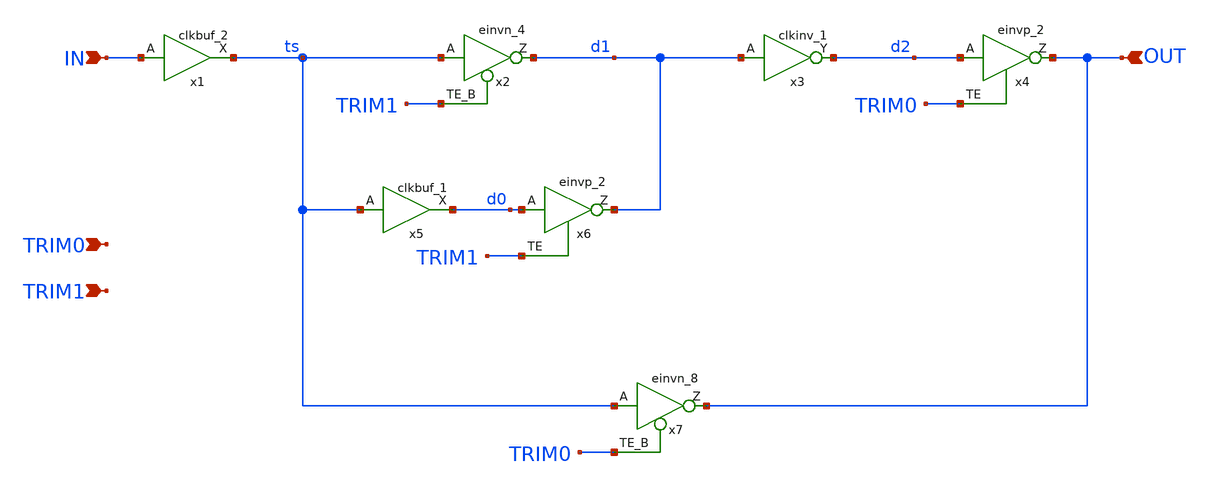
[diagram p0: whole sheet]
** sch_path: ip/randsack/sch/triminv.sch
**.subckt triminv IN OUT TRIM0 TRIM1
*.ipin IN
*.ipin OUT
*.ipin TRIM0
*.ipin TRIM1
x1 IN VGND VNB VPB VPWR ts sky130_fd_sc_hd__clkbuf_2
x2 ts TRIM1 VGND VNB VPB VPWR d1 sky130_fd_sc_hd__einvn_4
x3 d1 VGND VNB VPB VPWR d2 sky130_fd_sc_hd__clkinv_1
x4 d2 TRIM0 VGND VNB VPB VPWR OUT sky130_fd_sc_hd__einvp_2
x5 ts VGND VNB VPB VPWR d0 sky130_fd_sc_hd__clkbuf_1
x6 d0 TRIM1 VGND VNB VPB VPWR d1 sky130_fd_sc_hd__einvp_2
x7 ts TRIM0 VGND VNB VPB VPWR OUT sky130_fd_sc_hd__einvn_8
**.ends
.end
